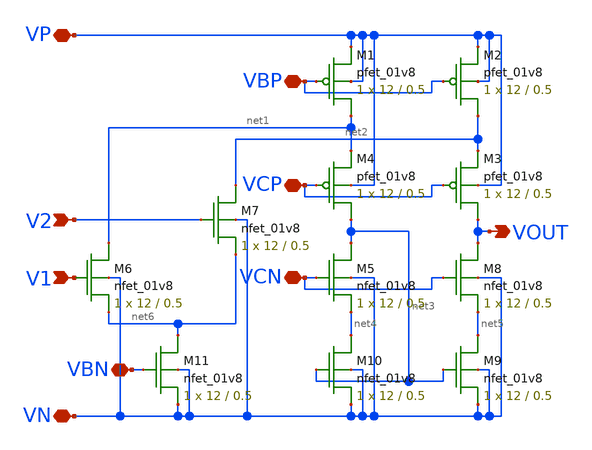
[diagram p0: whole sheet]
** sch_path: mp3/schematics/diff_amp.sch
**.subckt diff_amp V1 V2 VP VN VOUT VBP VCP VCN VBN
*.ipin V1
*.ipin V2
*.iopin VP
*.iopin VN
*.opin VOUT
*.iopin VBP
*.iopin VCP
*.iopin VCN
*.iopin VBN
XM1 net1 VBP VP VP sky130_fd_pr__pfet_01v8 L=0.5 W=12 nf=1 ad='int((nf+1)/2) * W/nf * 0.29' as='int((nf+2)/2) * W/nf * 0.29'
+ pd='2*int((nf+1)/2) * (W/nf + 0.29)' ps='2*int((nf+2)/2) * (W/nf + 0.29)' nrd='0.29 / W' nrs='0.29 / W'
+ sa=0 sb=0 sd=0 mult=1 m=1
XM5 net3 VCN net4 VN sky130_fd_pr__nfet_01v8 L=0.5 W=12 nf=1 ad='int((nf+1)/2) * W/nf * 0.29' as='int((nf+2)/2) * W/nf * 0.29'
+ pd='2*int((nf+1)/2) * (W/nf + 0.29)' ps='2*int((nf+2)/2) * (W/nf + 0.29)' nrd='0.29 / W' nrs='0.29 / W'
+ sa=0 sb=0 sd=0 mult=1 m=1
XM2 net2 VBP VP VP sky130_fd_pr__pfet_01v8 L=0.5 W=12 nf=1 ad='int((nf+1)/2) * W/nf * 0.29' as='int((nf+2)/2) * W/nf * 0.29'
+ pd='2*int((nf+1)/2) * (W/nf + 0.29)' ps='2*int((nf+2)/2) * (W/nf + 0.29)' nrd='0.29 / W' nrs='0.29 / W'
+ sa=0 sb=0 sd=0 mult=1 m=1
XM3 VOUT VCP net2 VP sky130_fd_pr__pfet_01v8 L=0.5 W=12 nf=1 ad='int((nf+1)/2) * W/nf * 0.29' as='int((nf+2)/2) * W/nf * 0.29'
+ pd='2*int((nf+1)/2) * (W/nf + 0.29)' ps='2*int((nf+2)/2) * (W/nf + 0.29)' nrd='0.29 / W' nrs='0.29 / W'
+ sa=0 sb=0 sd=0 mult=1 m=1
XM4 net3 VCP net1 VP sky130_fd_pr__pfet_01v8 L=0.5 W=12 nf=1 ad='int((nf+1)/2) * W/nf * 0.29' as='int((nf+2)/2) * W/nf * 0.29'
+ pd='2*int((nf+1)/2) * (W/nf + 0.29)' ps='2*int((nf+2)/2) * (W/nf + 0.29)' nrd='0.29 / W' nrs='0.29 / W'
+ sa=0 sb=0 sd=0 mult=1 m=1
XM6 net1 V1 net6 VN sky130_fd_pr__nfet_01v8 L=0.5 W=12 nf=1 ad='int((nf+1)/2) * W/nf * 0.29' as='int((nf+2)/2) * W/nf * 0.29'
+ pd='2*int((nf+1)/2) * (W/nf + 0.29)' ps='2*int((nf+2)/2) * (W/nf + 0.29)' nrd='0.29 / W' nrs='0.29 / W'
+ sa=0 sb=0 sd=0 mult=1 m=1
XM7 net2 V2 net6 VN sky130_fd_pr__nfet_01v8 L=0.5 W=12 nf=1 ad='int((nf+1)/2) * W/nf * 0.29' as='int((nf+2)/2) * W/nf * 0.29'
+ pd='2*int((nf+1)/2) * (W/nf + 0.29)' ps='2*int((nf+2)/2) * (W/nf + 0.29)' nrd='0.29 / W' nrs='0.29 / W'
+ sa=0 sb=0 sd=0 mult=1 m=1
XM8 VOUT VCN net5 VN sky130_fd_pr__nfet_01v8 L=0.5 W=12 nf=1 ad='int((nf+1)/2) * W/nf * 0.29' as='int((nf+2)/2) * W/nf * 0.29'
+ pd='2*int((nf+1)/2) * (W/nf + 0.29)' ps='2*int((nf+2)/2) * (W/nf + 0.29)' nrd='0.29 / W' nrs='0.29 / W'
+ sa=0 sb=0 sd=0 mult=1 m=1
XM9 net5 net3 VN VN sky130_fd_pr__nfet_01v8 L=0.5 W=12 nf=1 ad='int((nf+1)/2) * W/nf * 0.29' as='int((nf+2)/2) * W/nf * 0.29'
+ pd='2*int((nf+1)/2) * (W/nf + 0.29)' ps='2*int((nf+2)/2) * (W/nf + 0.29)' nrd='0.29 / W' nrs='0.29 / W'
+ sa=0 sb=0 sd=0 mult=1 m=1
XM10 net4 net3 VN VN sky130_fd_pr__nfet_01v8 L=0.5 W=12 nf=1 ad='int((nf+1)/2) * W/nf * 0.29' as='int((nf+2)/2) * W/nf * 0.29'
+ pd='2*int((nf+1)/2) * (W/nf + 0.29)' ps='2*int((nf+2)/2) * (W/nf + 0.29)' nrd='0.29 / W' nrs='0.29 / W'
+ sa=0 sb=0 sd=0 mult=1 m=1
XM11 net6 VBN VN VN sky130_fd_pr__nfet_01v8 L=0.5 W=12 nf=1 ad='int((nf+1)/2) * W/nf * 0.29' as='int((nf+2)/2) * W/nf * 0.29'
+ pd='2*int((nf+1)/2) * (W/nf + 0.29)' ps='2*int((nf+2)/2) * (W/nf + 0.29)' nrd='0.29 / W' nrs='0.29 / W'
+ sa=0 sb=0 sd=0 mult=1 m=1
**.ends
.end
